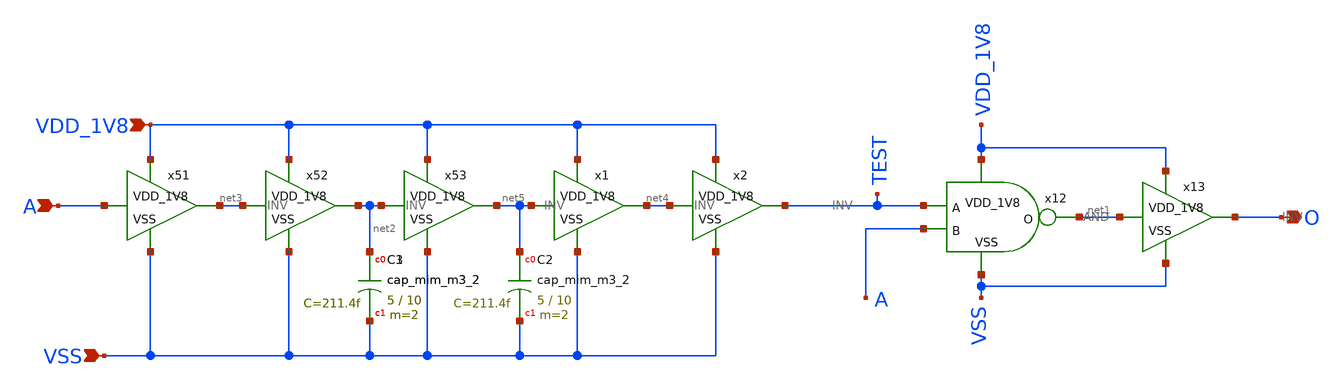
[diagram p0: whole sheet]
** sch_path: design/CNR_GR05_SKY130NM/POSEDGE.sch
**.subckt POSEDGE O VDD_1V8 VSS A
*.opin O
*.ipin VDD_1V8
*.ipin VSS
*.ipin A
x12 VDD_1V8 TEST A net1 VSS AND
x13 VDD_1V8 net1 O VSS INV
x51 VDD_1V8 A net3 VSS INV
x52 VDD_1V8 net3 net2 VSS INV
x53 VDD_1V8 net2 net5 VSS INV
x1 VDD_1V8 net5 net4 VSS INV
x2 VDD_1V8 net4 TEST VSS INV
XC3 net2 VSS sky130_fd_pr__cap_mim_m3_2 W=5 L=10 MF=2 m=2
XC1 net2 VSS sky130_fd_pr__cap_mim_m3_2 W=5 L=10 MF=2 m=2
XC2 net5 VSS sky130_fd_pr__cap_mim_m3_2 W=5 L=10 MF=2 m=2
**.ends
.end
